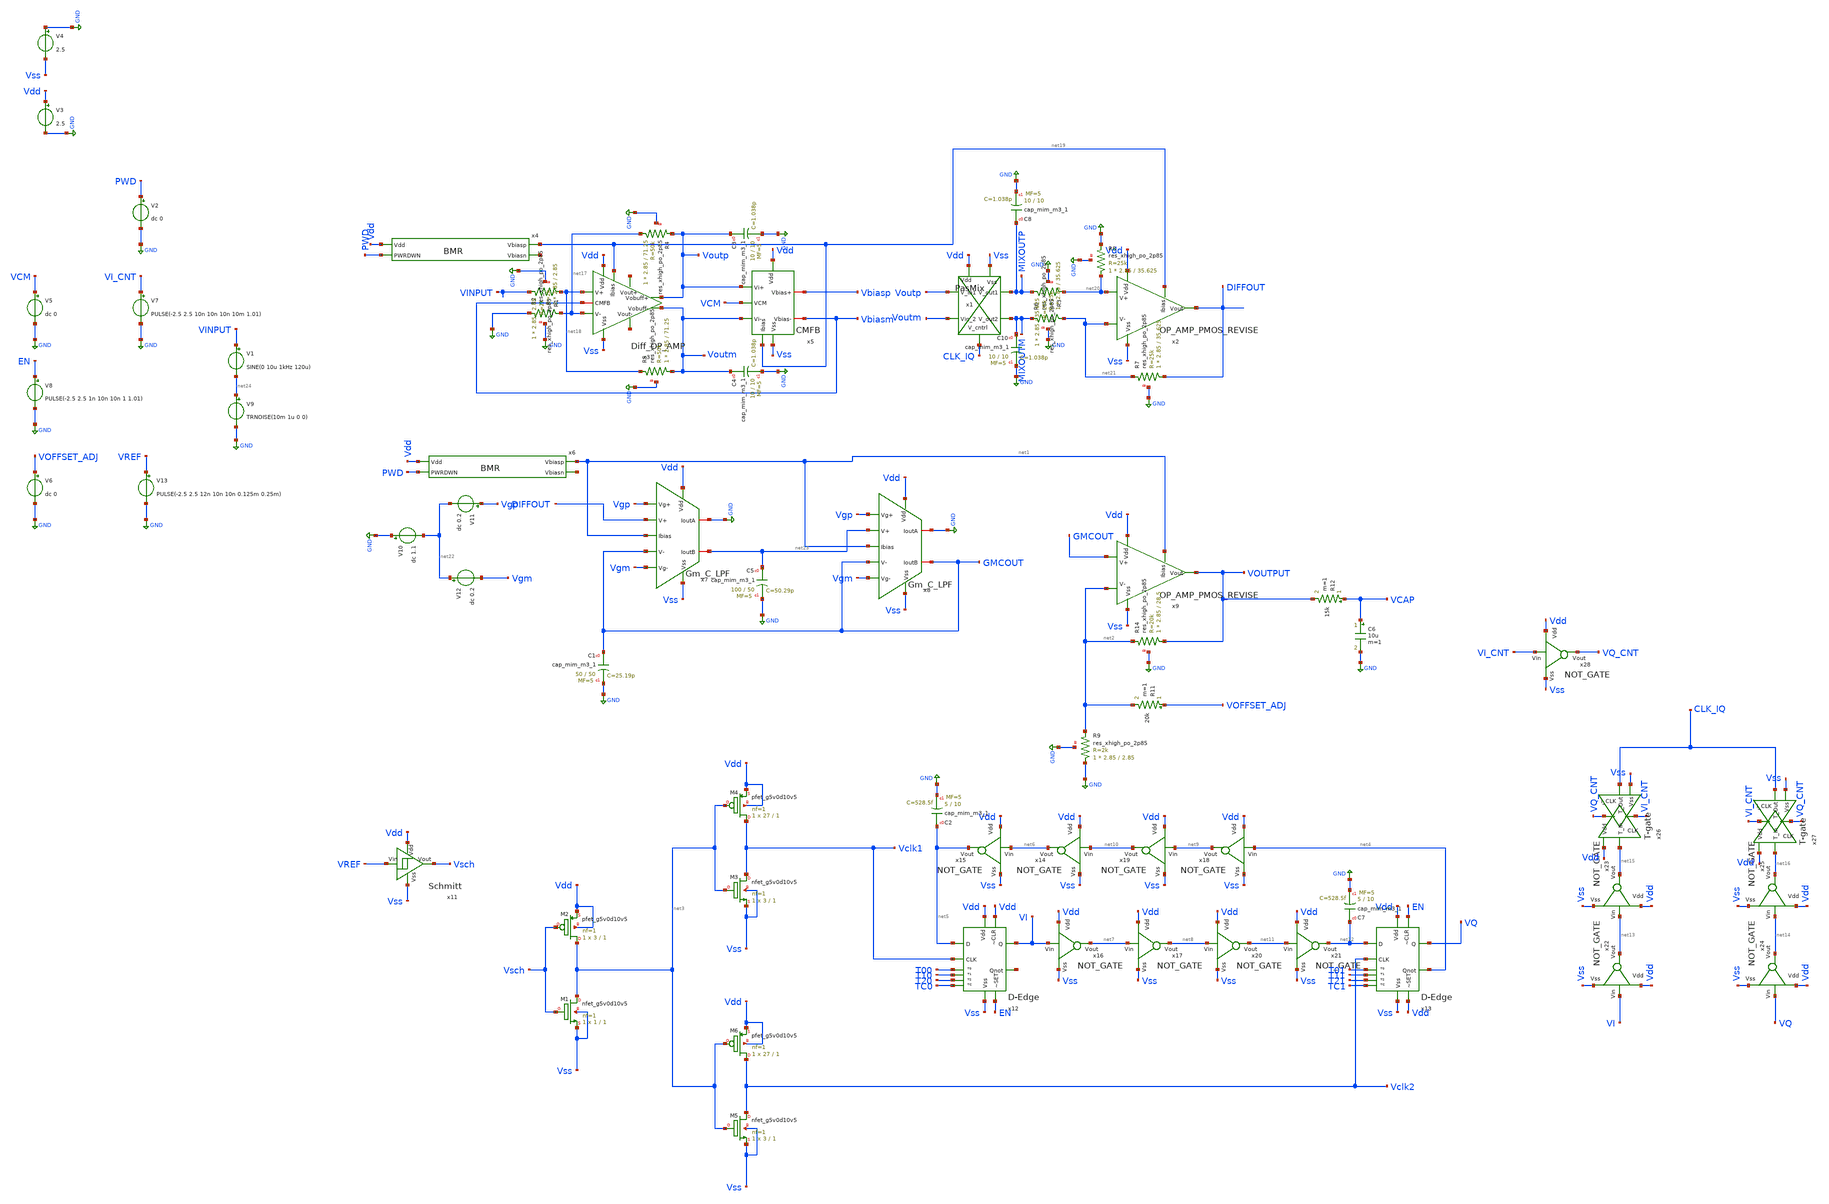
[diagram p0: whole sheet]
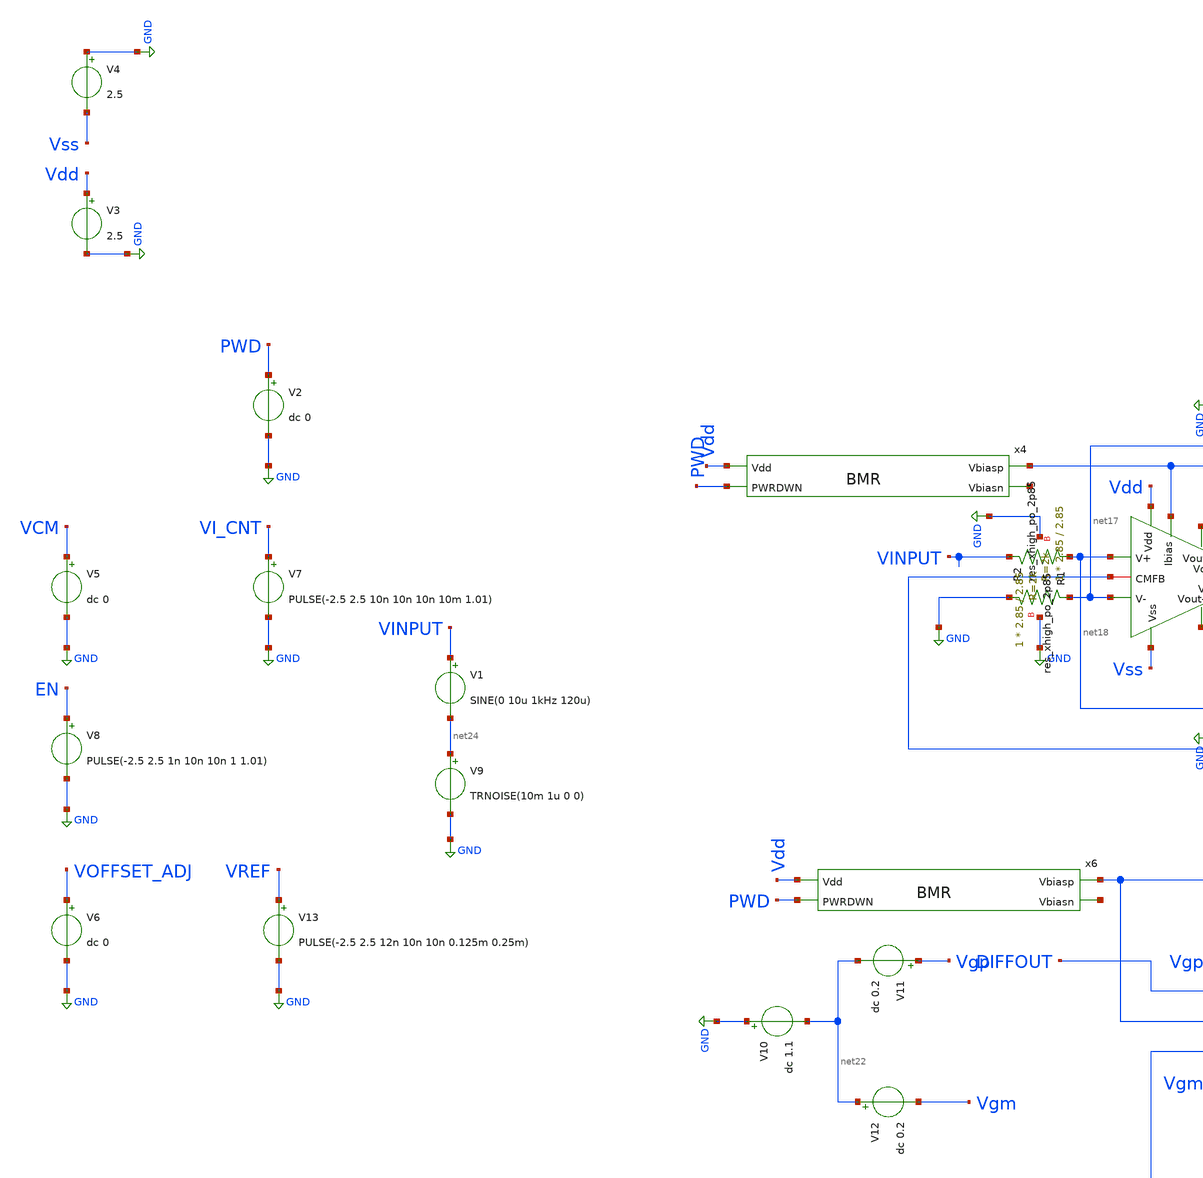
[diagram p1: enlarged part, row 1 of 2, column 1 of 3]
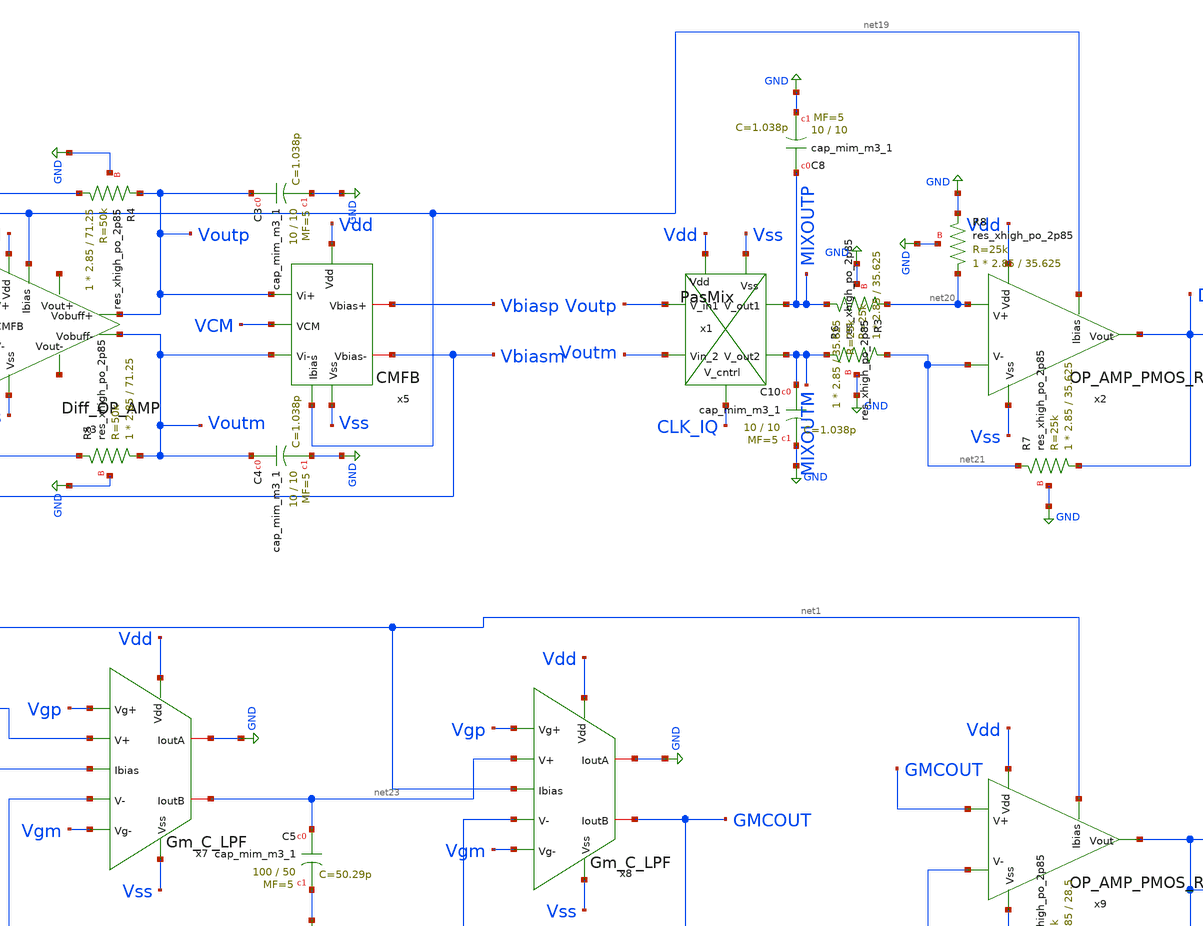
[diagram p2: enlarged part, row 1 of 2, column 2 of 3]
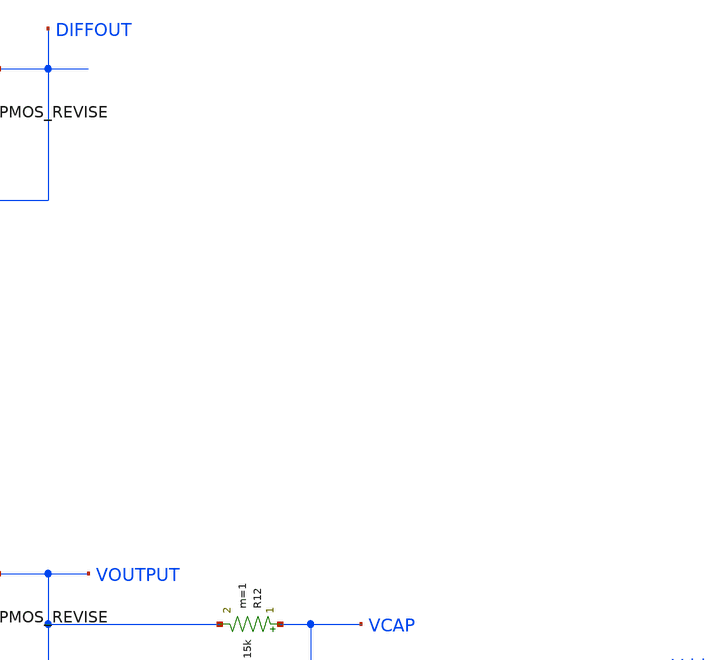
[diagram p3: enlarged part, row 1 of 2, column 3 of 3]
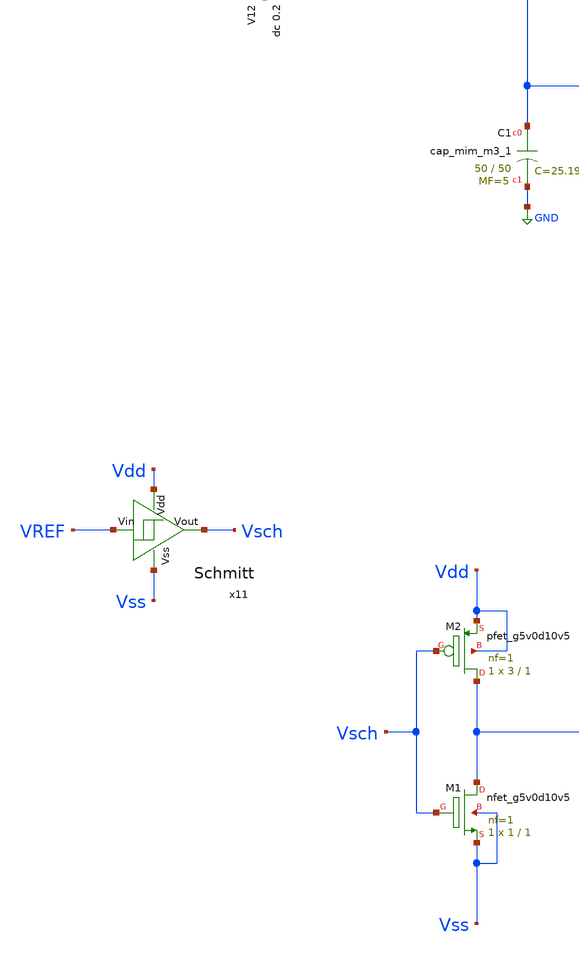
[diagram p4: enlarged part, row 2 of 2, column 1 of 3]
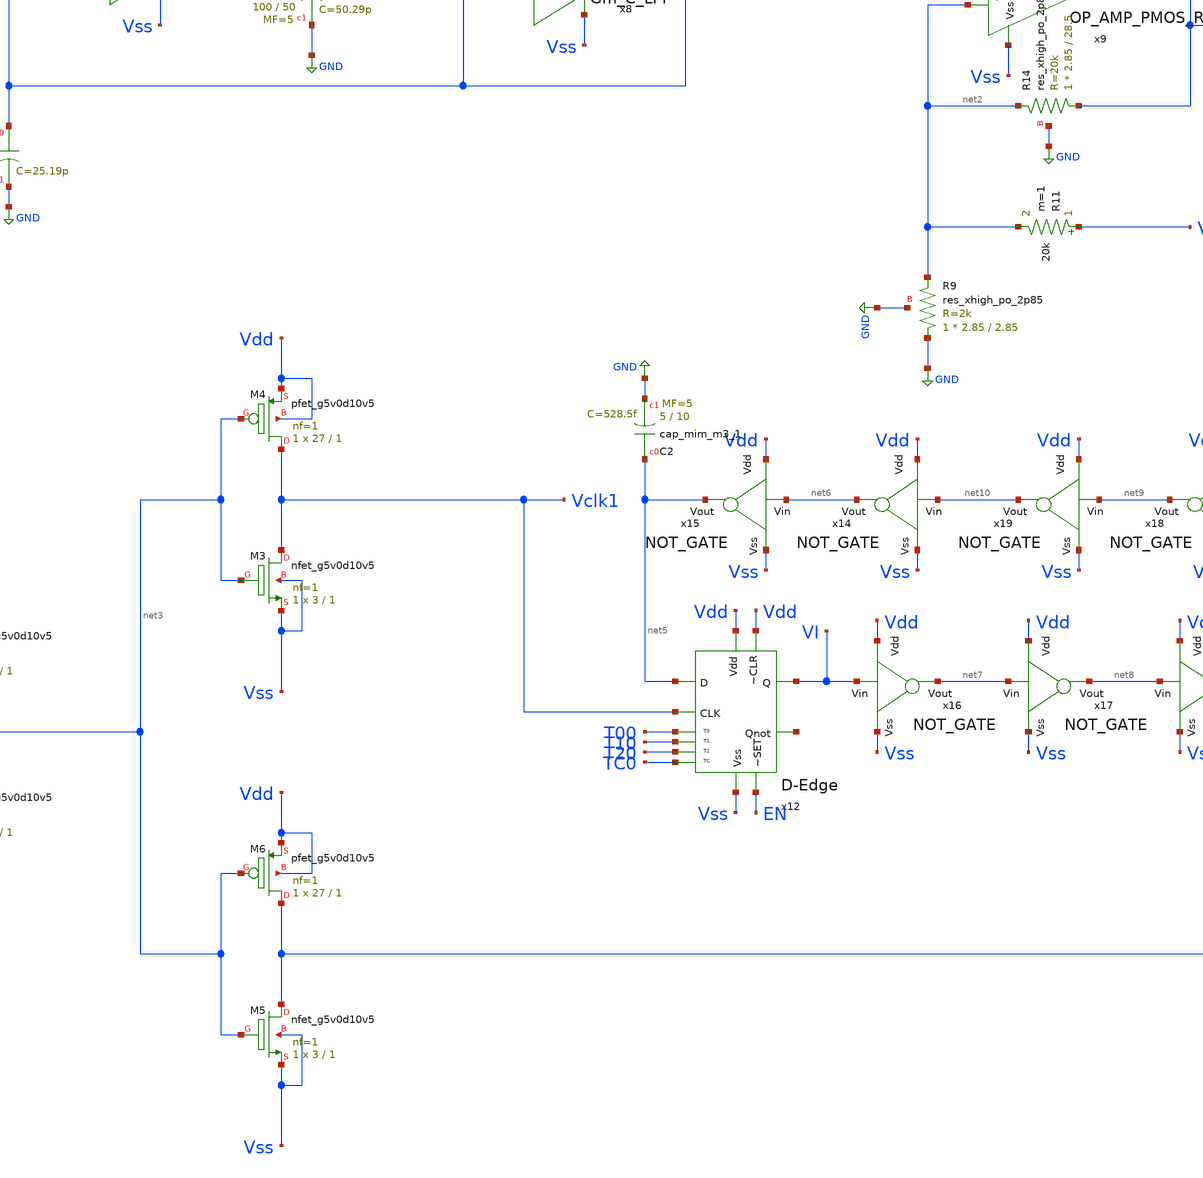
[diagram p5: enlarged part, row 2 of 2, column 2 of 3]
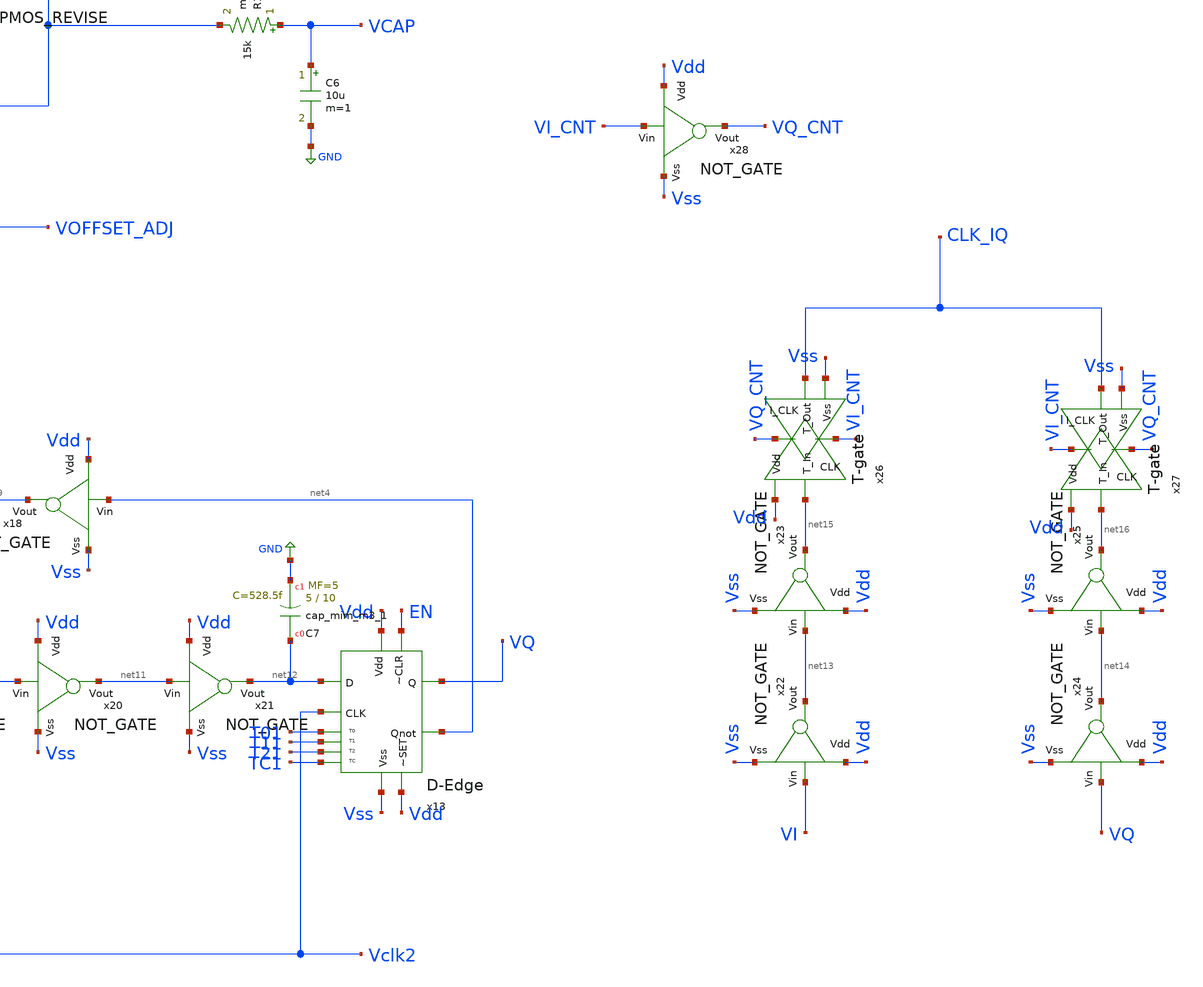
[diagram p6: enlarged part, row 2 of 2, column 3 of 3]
** sch_path: xschem/Lock_In_Amplifier.sch
**.subckt Lock_In_Amplifier
V1 VINPUT net24 SINE(0 10u 1kHz 120u)
V4 GND Vss 2.5
V3 Vdd GND 2.5
V5 VCM GND dc 0
x9 Vdd Vss net1 VOUTPUT GMCOUT net2 OP_AMP_PMOS_REVISE
V2 PWD GND dc 0
x11 Vdd Vss VREF Vsch Schmitt
V13 VREF GND PULSE(-2.5 2.5 12n 10n 10n 0.125m 0.25m)
XM1 net3 Vsch Vss Vss sky130_fd_pr__nfet_g5v0d10v5 L=1 W=1 nf=1 ad='int((1 + 1)/2) * 1 / 1 * 0.29' as='int((1 + 2)/2) * 1 / 1 * 0.29'
+ pd='2*int((1 + 1)/2) * (1 / 1 + 0.29)' ps='2*int((1 + 2)/2) * (1 / 1 + 0.29)' nrd='0.29 / 1 ' nrs='0.29 / 1 '
+ sa=0 sb=0 sd=0 mult=1 m=1
XM2 net3 Vsch Vdd Vdd sky130_fd_pr__pfet_g5v0d10v5 L=1 W=3 nf=1 ad='int((1 + 1)/2) * 3 / 1 * 0.29' as='int((1 + 2)/2) * 3 / 1 * 0.29'
+ pd='2*int((1 + 1)/2) * (3 / 1 + 0.29)' ps='2*int((1 + 2)/2) * (3 / 1 + 0.29)' nrd='0.29 / 3 ' nrs='0.29 / 3 '
+ sa=0 sb=0 sd=0 mult=1 m=1
XM3 Vclk1 net3 Vss Vss sky130_fd_pr__nfet_g5v0d10v5 L=1 W=3 nf=1 ad='int((1 + 1)/2) * 3 / 1 * 0.29' as='int((1 + 2)/2) * 3 / 1 * 0.29'
+ pd='2*int((1 + 1)/2) * (3 / 1 + 0.29)' ps='2*int((1 + 2)/2) * (3 / 1 + 0.29)' nrd='0.29 / 3 ' nrs='0.29 / 3 '
+ sa=0 sb=0 sd=0 mult=1 m=1
XM4 Vclk1 net3 Vdd Vdd sky130_fd_pr__pfet_g5v0d10v5 L=1 W=27 nf=1 ad='int((1 + 1)/2) * 27 / 1 * 0.29'
+ as='int((1 + 2)/2) * 27 / 1 * 0.29' pd='2*int((1 + 1)/2) * (27 / 1 + 0.29)' ps='2*int((1 + 2)/2) * (27 / 1 + 0.29)'
+ nrd='0.29 / 27 ' nrs='0.29 / 27 ' sa=0 sb=0 sd=0 mult=1 m=1
XM5 Vclk2 net3 Vss Vss sky130_fd_pr__nfet_g5v0d10v5 L=1 W=3 nf=1 ad='int((1 + 1)/2) * 3 / 1 * 0.29' as='int((1 + 2)/2) * 3 / 1 * 0.29'
+ pd='2*int((1 + 1)/2) * (3 / 1 + 0.29)' ps='2*int((1 + 2)/2) * (3 / 1 + 0.29)' nrd='0.29 / 3 ' nrs='0.29 / 3 '
+ sa=0 sb=0 sd=0 mult=1 m=1
XM6 Vclk2 net3 Vdd Vdd sky130_fd_pr__pfet_g5v0d10v5 L=1 W=27 nf=1 ad='int((1 + 1)/2) * 27 / 1 * 0.29'
+ as='int((1 + 2)/2) * 27 / 1 * 0.29' pd='2*int((1 + 1)/2) * (27 / 1 + 0.29)' ps='2*int((1 + 2)/2) * (27 / 1 + 0.29)'
+ nrd='0.29 / 27 ' nrs='0.29 / 27 ' sa=0 sb=0 sd=0 mult=1 m=1
x12 Vdd Vss Vdd EN VI net5 net25 Vclk1 TC0 T20 T10 T00 D-Edge
x13 Vdd Vss EN Vdd VQ net12 net4 Vclk2 TC1 T21 T11 T01 D-Edge
x14 Vdd net6 net10 Vss NOT_GATE
x15 Vdd net5 net6 Vss NOT_GATE
x16 Vdd net7 VI Vss NOT_GATE
x17 Vdd net8 net7 Vss NOT_GATE
x18 Vdd net9 net4 Vss NOT_GATE
x19 Vdd net10 net9 Vss NOT_GATE
x20 Vdd net11 net8 Vss NOT_GATE
x21 Vdd net12 net11 Vss NOT_GATE
V8 EN GND PULSE(-2.5 2.5 1n 10n 10n 1 1.01)
x22 Vdd net13 VI Vss NOT_GATE
x23 Vdd net15 net13 Vss NOT_GATE
x24 Vdd net14 VQ Vss NOT_GATE
x25 Vdd net16 net14 Vss NOT_GATE
x26 VQ_CNT net15 CLK_IQ Vdd Vss VI_CNT T-gate
x27 VI_CNT net16 CLK_IQ Vdd Vss VQ_CNT T-gate
x28 Vdd VQ_CNT VI_CNT Vss NOT_GATE
V6 VOFFSET_ADJ GND dc 0
x3 Vss Vbiasm net26 net27 net17 net18 Voutp Voutm net19 Vdd Diff_OP_AMP
x4 Vdd net19 net28 PWD BMR
x5 Vss Vbiasp Vbiasm Voutm Voutp VCM net19 Vdd CMFB
x1 Vdd CLK_IQ Vss MIXOUTP Voutp MIXOUTM Voutm PasMix
x2 Vdd Vss net19 DIFFOUT net20 net21 OP_AMP_PMOS_REVISE
V7 VI_CNT GND PULSE(-2.5 2.5 10n 10n 10n 10m 1.01)
V10 GND net22 dc 1.1
V11 Vgp net22 dc 0.2
x6 Vdd net1 net29 PWD BMR
x7 Vdd Vss Vgp Vgm GND net23 DIFFOUT GMCOUT net1 Gm_C_LPF
V12 net22 Vgm dc 0.2
x8 Vdd Vss Vgp Vgm GND GMCOUT net23 GMCOUT net1 Gm_C_LPF
R11 VOFFSET_ADJ net2 20k m=1
V9 net24 GND TRNOISE(10m 1u 0 0)
R12 VCAP VOUTPUT 15k m=1
C6 VCAP GND 10u m=1
XC3 Voutp GND sky130_fd_pr__cap_mim_m3_1 W=10 L=10 MF=5 m=5
XC4 Voutm GND sky130_fd_pr__cap_mim_m3_1 W=10 L=10 MF=5 m=5
XR4 net17 Voutp GND sky130_fd_pr__res_xhigh_po_2p85 L=71.25 mult=1 m=1
XR5 Voutm net18 GND sky130_fd_pr__res_xhigh_po_2p85 L=71.25 mult=1 m=1
XR2 net17 GND GND sky130_fd_pr__res_xhigh_po_2p85 L=2.85 mult=1 m=1
XR1 VINPUT net18 GND sky130_fd_pr__res_xhigh_po_2p85 L=2.85 mult=1 m=1
XC10 MIXOUTM GND sky130_fd_pr__cap_mim_m3_1 W=10 L=10 MF=5 m=5
XC8 MIXOUTP GND sky130_fd_pr__cap_mim_m3_1 W=10 L=10 MF=5 m=5
XC2 net5 GND sky130_fd_pr__cap_mim_m3_1 W=5 L=10 MF=5 m=5
XC7 net12 GND sky130_fd_pr__cap_mim_m3_1 W=5 L=10 MF=5 m=5
XR7 DIFFOUT net21 GND sky130_fd_pr__res_xhigh_po_2p85 L=35.625 mult=1 m=1
XR6 net21 MIXOUTM GND sky130_fd_pr__res_xhigh_po_2p85 L=35.625 mult=1 m=1
XR3 MIXOUTP net20 GND sky130_fd_pr__res_xhigh_po_2p85 L=35.625 mult=1 m=1
XR8 net20 GND GND sky130_fd_pr__res_xhigh_po_2p85 L=35.625 mult=1 m=1
XC5 net23 GND sky130_fd_pr__cap_mim_m3_1 W=100 L=50 MF=5 m=5
XC1 GMCOUT GND sky130_fd_pr__cap_mim_m3_1 W=50 L=50 MF=5 m=5
XR9 GND net2 GND sky130_fd_pr__res_xhigh_po_2p85 L=2.85 mult=1 m=1
XR14 VOUTPUT net2 GND sky130_fd_pr__res_xhigh_po_2p85 L=28.5 mult=1 m=1
**** begin user architecture code






.lib /foss/pdks/sky130A/libs.tech/combined/sky130.lib.spice tt
.options method = trap
.options rshunt = 1e12
.options retol = 0.01
.options vntol = 10u
.options abstol = 1n
.options trtol = 10
.options chgtol = 1e-10

.options sparse
.control
 save v(VOUTPUT) v(GMCOUT) v(VCAP)
 tran 1u 1 0 100u

 write Lock_In_Amplifier_TB_TT_NOISY_10UV_0.4_1S_FFT_NGSPICE.raw
 ***write Lock_In_Amplifier_TB_TT_1MV_IDEAL_NGSPICE.raw


 set appendwrite
.endc
.end


**** end user architecture code
**.ends

* expanding   symbol:  OP_AMP_PMOS_REVISE.sym # of pins=6
** sym_path: xschem/OP_AMP_PMOS_REVISE.sym
** sch_path: xschem/OP_AMP_PMOS_REVISE.sch
.subckt OP_AMP_PMOS_REVISE Vdd Vss Ibias Vout V+ V-
*.ipin V-
*.ipin V+
*.ipin Vdd
*.ipin Vss
*.ipin Ibias
*.opin Vout
XM3 net2 net1 Vss Vss sky130_fd_pr__nfet_g5v0d10v5 L=6 W=0.81 nf=1 ad='int((1 + 1)/2) * 0.81 / 1 * 0.29'
+ as='int((1 + 2)/2) * 0.81 / 1 * 0.29' pd='2*int((1 + 1)/2) * (0.81 / 1 + 0.29)' ps='2*int((1 + 2)/2) * (0.81 / 1 + 0.29)'
+ nrd='0.29 / 0.81 ' nrs='0.29 / 0.81 ' sa=0 sb=0 sd=0 mult=2 m=2
XM1 net2 V+ net3 net3 sky130_fd_pr__pfet_g5v0d10v5 L=3 W=80 nf=8 ad='int((8 + 1)/2) * 80 / 8 * 0.29'
+ as='int((8 + 2)/2) * 80 / 8 * 0.29' pd='2*int((8 + 1)/2) * (80 / 8 + 0.29)' ps='2*int((8 + 2)/2) * (80 / 8 + 0.29)'
+ nrd='0.29 / 80 ' nrs='0.29 / 80 ' sa=0 sb=0 sd=0 mult=4 m=4
XM2 net1 V- net3 net3 sky130_fd_pr__pfet_g5v0d10v5 L=3 W=80 nf=8 ad='int((8 + 1)/2) * 80 / 8 * 0.29'
+ as='int((8 + 2)/2) * 80 / 8 * 0.29' pd='2*int((8 + 1)/2) * (80 / 8 + 0.29)' ps='2*int((8 + 2)/2) * (80 / 8 + 0.29)'
+ nrd='0.29 / 80 ' nrs='0.29 / 80 ' sa=0 sb=0 sd=0 mult=4 m=4
XM4 net1 net1 Vss Vss sky130_fd_pr__nfet_g5v0d10v5 L=6 W=0.81 nf=1 ad='int((1 + 1)/2) * 0.81 / 1 * 0.29'
+ as='int((1 + 2)/2) * 0.81 / 1 * 0.29' pd='2*int((1 + 1)/2) * (0.81 / 1 + 0.29)' ps='2*int((1 + 2)/2) * (0.81 / 1 + 0.29)'
+ nrd='0.29 / 0.81 ' nrs='0.29 / 0.81 ' sa=0 sb=0 sd=0 mult=2 m=2
XM8 net4 net2 Vss Vss sky130_fd_pr__nfet_g5v0d10v5 L=3 W=14 nf=4 ad='int((4 + 1)/2) * 14 / 4 * 0.29'
+ as='int((4 + 2)/2) * 14 / 4 * 0.29' pd='2*int((4 + 1)/2) * (14 / 4 + 0.29)' ps='2*int((4 + 2)/2) * (14 / 4 + 0.29)'
+ nrd='0.29 / 14 ' nrs='0.29 / 14 ' sa=0 sb=0 sd=0 mult=2 m=2
XM5 net3 Ibias Vdd Vdd sky130_fd_pr__pfet_g5v0d10v5 L=3 W=31 nf=8 ad='int((8 + 1)/2) * 31 / 8 * 0.29'
+ as='int((8 + 2)/2) * 31 / 8 * 0.29' pd='2*int((8 + 1)/2) * (31 / 8 + 0.29)' ps='2*int((8 + 2)/2) * (31 / 8 + 0.29)'
+ nrd='0.29 / 31 ' nrs='0.29 / 31 ' sa=0 sb=0 sd=0 mult=2 m=2
XM6 net6 Ibias Vdd Vdd sky130_fd_pr__pfet_g5v0d10v5 L=3 W=31 nf=8 ad='int((8 + 1)/2) * 31 / 8 * 0.29'
+ as='int((8 + 2)/2) * 31 / 8 * 0.29' pd='2*int((8 + 1)/2) * (31 / 8 + 0.29)' ps='2*int((8 + 2)/2) * (31 / 8 + 0.29)'
+ nrd='0.29 / 31 ' nrs='0.29 / 31 ' sa=0 sb=0 sd=0 mult=30 m=30
XM7 net4 net4 net5 net5 sky130_fd_pr__pfet_g5v0d10v5 L=3 W=41.1 nf=4 ad='int((4 + 1)/2) * 41.1 / 4 * 0.29'
+ as='int((4 + 2)/2) * 41.1 / 4 * 0.29' pd='2*int((4 + 1)/2) * (41.1 / 4 + 0.29)' ps='2*int((4 + 2)/2) * (41.1 / 4 + 0.29)'
+ nrd='0.29 / 41.1 ' nrs='0.29 / 41.1 ' sa=0 sb=0 sd=0 mult=4 m=4
XM9 Vss net4 Vout Vout sky130_fd_pr__pfet_g5v0d10v5 L=3 W=41.1 nf=4 ad='int((4 + 1)/2) * 41.1 / 4 * 0.29'
+ as='int((4 + 2)/2) * 41.1 / 4 * 0.29' pd='2*int((4 + 1)/2) * (41.1 / 4 + 0.29)' ps='2*int((4 + 2)/2) * (41.1 / 4 + 0.29)'
+ nrd='0.29 / 41.1 ' nrs='0.29 / 41.1 ' sa=0 sb=0 sd=0 mult=4 m=4
XM10 net6 net6 net5 net5 sky130_fd_pr__nfet_g5v0d10v5 L=3 W=18 nf=4 ad='int((4 + 1)/2) * 18 / 4 * 0.29'
+ as='int((4 + 2)/2) * 18 / 4 * 0.29' pd='2*int((4 + 1)/2) * (18 / 4 + 0.29)' ps='2*int((4 + 2)/2) * (18 / 4 + 0.29)'
+ nrd='0.29 / 18 ' nrs='0.29 / 18 ' sa=0 sb=0 sd=0 mult=2 m=2
XM11 Vdd net6 Vout Vout sky130_fd_pr__nfet_g5v0d10v5 L=3 W=18 nf=4 ad='int((4 + 1)/2) * 18 / 4 * 0.29'
+ as='int((4 + 2)/2) * 18 / 4 * 0.29' pd='2*int((4 + 1)/2) * (18 / 4 + 0.29)' ps='2*int((4 + 2)/2) * (18 / 4 + 0.29)'
+ nrd='0.29 / 18 ' nrs='0.29 / 18 ' sa=0 sb=0 sd=0 mult=2 m=2
XC10 net2 net4 sky130_fd_pr__cap_mim_m3_1 W=10 L=10 MF=5 m=5
.ends


* expanding   symbol:  Schmitt.sym # of pins=4
** sym_path: xschem/Schmitt.sym
** sch_path: xschem/Schmitt.sch
.subckt Schmitt Vdd Vss Vin Vout
*.opin Vout
*.ipin Vin
*.ipin Vdd
*.ipin Vss
XM1 net1 Vin Vss Vss sky130_fd_pr__nfet_g5v0d10v5 L=0.5 W=2.92 nf=1 ad='int((1 + 1)/2) * 2.92 / 1 * 0.29'
+ as='int((1 + 2)/2) * 2.92 / 1 * 0.29' pd='2*int((1 + 1)/2) * (2.92 / 1 + 0.29)' ps='2*int((1 + 2)/2) * (2.92 / 1 + 0.29)'
+ nrd='0.29 / 2.92 ' nrs='0.29 / 2.92 ' sa=0 sb=0 sd=0 mult=1 m=1
XM5 net2 Vin Vdd Vdd sky130_fd_pr__pfet_g5v0d10v5 L=0.5 W=9.78 nf=1 ad='int((1 + 1)/2) * 9.78 / 1 * 0.29'
+ as='int((1 + 2)/2) * 9.78 / 1 * 0.29' pd='2*int((1 + 1)/2) * (9.78 / 1 + 0.29)' ps='2*int((1 + 2)/2) * (9.78 / 1 + 0.29)'
+ nrd='0.29 / 9.78 ' nrs='0.29 / 9.78 ' sa=0 sb=0 sd=0 mult=1 m=1
XM3 Vdd Vout net1 Vss sky130_fd_pr__nfet_g5v0d10v5 L=0.5 W=1 nf=1 ad='int((1 + 1)/2) * 1 / 1 * 0.29'
+ as='int((1 + 2)/2) * 1 / 1 * 0.29' pd='2*int((1 + 1)/2) * (1 / 1 + 0.29)' ps='2*int((1 + 2)/2) * (1 / 1 + 0.29)'
+ nrd='0.29 / 1 ' nrs='0.29 / 1 ' sa=0 sb=0 sd=0 mult=1 m=1
XM2 Vout Vin net1 Vss sky130_fd_pr__nfet_g5v0d10v5 L=0.5 W=4 nf=1 ad='int((1 + 1)/2) * 4 / 1 * 0.29'
+ as='int((1 + 2)/2) * 4 / 1 * 0.29' pd='2*int((1 + 1)/2) * (4 / 1 + 0.29)' ps='2*int((1 + 2)/2) * (4 / 1 + 0.29)'
+ nrd='0.29 / 4 ' nrs='0.29 / 4 ' sa=0 sb=0 sd=0 mult=1 m=1
XM6 Vss Vout net2 Vdd sky130_fd_pr__pfet_g5v0d10v5 L=0.5 W=3 nf=1 ad='int((1 + 1)/2) * 3 / 1 * 0.29'
+ as='int((1 + 2)/2) * 3 / 1 * 0.29' pd='2*int((1 + 1)/2) * (3 / 1 + 0.29)' ps='2*int((1 + 2)/2) * (3 / 1 + 0.29)'
+ nrd='0.29 / 3 ' nrs='0.29 / 3 ' sa=0 sb=0 sd=0 mult=1 m=1
XM4 Vout Vin net2 Vdd sky130_fd_pr__pfet_g5v0d10v5 L=0.5 W=12 nf=1 ad='int((1 + 1)/2) * 12 / 1 * 0.29'
+ as='int((1 + 2)/2) * 12 / 1 * 0.29' pd='2*int((1 + 1)/2) * (12 / 1 + 0.29)' ps='2*int((1 + 2)/2) * (12 / 1 + 0.29)'
+ nrd='0.29 / 12 ' nrs='0.29 / 12 ' sa=0 sb=0 sd=0 mult=1 m=1
.ends


* expanding   symbol:  D-Edge.sym # of pins=12
** sym_path: xschem/D-Edge.sym
** sch_path: xschem/D-Edge.sch
.subckt D-Edge Vdd Vss ~CLR ~SET Q D Qnot CLK TC T2 T1 T0
*.ipin D
*.ipin Vdd
*.ipin Vss
*.opin Q
*.opin Qnot
*.ipin ~CLR
*.ipin ~SET
*.ipin CLK
*.opin T0
*.opin T1
*.opin T2
*.opin TC
x1 CLK D T1 Vdd Vss CLK_I T-gate
x3 CLK_I T0 T1 Vdd Vss CLK T-gate
x4 CLK_I net1 T2 Vdd Vss CLK T-gate
x8 CLK Qnot T2 Vdd Vss CLK_I T-gate
x11 Vdd ~CLR T1 net1 Vss NAND_GATE
x2 Vdd ~SET net1 T0 Vss NAND_GATE
x5 Vdd ~CLR T2 Q Vss NAND_GATE
x7 Vdd ~SET Q Qnot Vss NAND_GATE
XM1 CLK_I CLK Vss Vss sky130_fd_pr__nfet_g5v0d10v5 L=1 W=3 nf=1 ad='int((1 + 1)/2) * 3 / 1 * 0.29' as='int((1 + 2)/2) * 3 / 1 * 0.29'
+ pd='2*int((1 + 1)/2) * (3 / 1 + 0.29)' ps='2*int((1 + 2)/2) * (3 / 1 + 0.29)' nrd='0.29 / 3 ' nrs='0.29 / 3 '
+ sa=0 sb=0 sd=0 mult=1 m=1
XM2 CLK_I CLK Vdd Vdd sky130_fd_pr__pfet_g5v0d10v5 L=1 W=27 nf=1 ad='int((1 + 1)/2) * 27 / 1 * 0.29'
+ as='int((1 + 2)/2) * 27 / 1 * 0.29' pd='2*int((1 + 1)/2) * (27 / 1 + 0.29)' ps='2*int((1 + 2)/2) * (27 / 1 + 0.29)'
+ nrd='0.29 / 27 ' nrs='0.29 / 27 ' sa=0 sb=0 sd=0 mult=1 m=1
XM3 TC CLK_I Vss Vss sky130_fd_pr__nfet_g5v0d10v5 L=1 W=3 nf=1 ad='int((1 + 1)/2) * 3 / 1 * 0.29' as='int((1 + 2)/2) * 3 / 1 * 0.29'
+ pd='2*int((1 + 1)/2) * (3 / 1 + 0.29)' ps='2*int((1 + 2)/2) * (3 / 1 + 0.29)' nrd='0.29 / 3 ' nrs='0.29 / 3 '
+ sa=0 sb=0 sd=0 mult=1 m=1
XM4 TC CLK_I Vdd Vdd sky130_fd_pr__pfet_g5v0d10v5 L=1 W=27 nf=1 ad='int((1 + 1)/2) * 27 / 1 * 0.29' as='int((1 + 2)/2) * 27 / 1 * 0.29'
+ pd='2*int((1 + 1)/2) * (27 / 1 + 0.29)' ps='2*int((1 + 2)/2) * (27 / 1 + 0.29)' nrd='0.29 / 27 ' nrs='0.29 / 27 '
+ sa=0 sb=0 sd=0 mult=1 m=1
.ends


* expanding   symbol:  NOT_GATE.sym # of pins=4
** sym_path: xschem/NOT_GATE.sym
** sch_path: xschem/NOT_GATE.sch
.subckt NOT_GATE Vdd Vout Vin Vss
*.opin Vout
*.ipin Vdd
*.ipin Vss
*.ipin Vin
XM1 Vout Vin Vss Vss sky130_fd_pr__nfet_g5v0d10v5 L=1 W=1 nf=1 ad='int((1 + 1)/2) * 1 / 1 * 0.29' as='int((1 + 2)/2) * 1 / 1 * 0.29'
+ pd='2*int((1 + 1)/2) * (1 / 1 + 0.29)' ps='2*int((1 + 2)/2) * (1 / 1 + 0.29)' nrd='0.29 / 1 ' nrs='0.29 / 1 '
+ sa=0 sb=0 sd=0 mult=1 m=1
XM2 Vout Vin Vdd Vdd sky130_fd_pr__pfet_g5v0d10v5 L=1 W=3 nf=1 ad='int((1 + 1)/2) * 3 / 1 * 0.29' as='int((1 + 2)/2) * 3 / 1 * 0.29'
+ pd='2*int((1 + 1)/2) * (3 / 1 + 0.29)' ps='2*int((1 + 2)/2) * (3 / 1 + 0.29)' nrd='0.29 / 3 ' nrs='0.29 / 3 '
+ sa=0 sb=0 sd=0 mult=1 m=1
.ends


* expanding   symbol:  T-gate.sym # of pins=6
** sym_path: xschem/T-gate.sym
** sch_path: xschem/T-gate.sch
.subckt T-gate I_CLK T_In T_Out Vdd Vss CLK
*.ipin T_In
*.opin T_Out
*.ipin Vdd
*.ipin Vss
*.ipin I_CLK
*.ipin CLK
XM1 T_In I_CLK T_Out Vdd sky130_fd_pr__pfet_g5v0d10v5 L=0.5 W=3 nf=1 ad='int((1 + 1)/2) * 3 / 1 * 0.29'
+ as='int((1 + 2)/2) * 3 / 1 * 0.29' pd='2*int((1 + 1)/2) * (3 / 1 + 0.29)' ps='2*int((1 + 2)/2) * (3 / 1 + 0.29)'
+ nrd='0.29 / 3 ' nrs='0.29 / 3 ' sa=0 sb=0 sd=0 mult=1 m=1
XM3 T_Out CLK T_In Vss sky130_fd_pr__nfet_g5v0d10v5 L=0.5 W=1 nf=1 ad='int((1 + 1)/2) * 1 / 1 * 0.29'
+ as='int((1 + 2)/2) * 1 / 1 * 0.29' pd='2*int((1 + 1)/2) * (1 / 1 + 0.29)' ps='2*int((1 + 2)/2) * (1 / 1 + 0.29)'
+ nrd='0.29 / 1 ' nrs='0.29 / 1 ' sa=0 sb=0 sd=0 mult=1 m=1
XM2 T_Out CLK T_Out Vdd sky130_fd_pr__pfet_g5v0d10v5 L=0.5 W=1.5 nf=1 ad='int((1 + 1)/2) * 1.5 / 1 * 0.29'
+ as='int((1 + 2)/2) * 1.5 / 1 * 0.29' pd='2*int((1 + 1)/2) * (1.5 / 1 + 0.29)' ps='2*int((1 + 2)/2) * (1.5 / 1 + 0.29)'
+ nrd='0.29 / 1.5 ' nrs='0.29 / 1.5 ' sa=0 sb=0 sd=0 mult=1 m=1
XM4 T_In CLK T_In Vdd sky130_fd_pr__pfet_g5v0d10v5 L=0.5 W=1.5 nf=1 ad='int((1 + 1)/2) * 1.5 / 1 * 0.29'
+ as='int((1 + 2)/2) * 1.5 / 1 * 0.29' pd='2*int((1 + 1)/2) * (1.5 / 1 + 0.29)' ps='2*int((1 + 2)/2) * (1.5 / 1 + 0.29)'
+ nrd='0.29 / 1.5 ' nrs='0.29 / 1.5 ' sa=0 sb=0 sd=0 mult=1 m=1
XM5 T_In I_CLK T_In Vss sky130_fd_pr__nfet_g5v0d10v5 L=0.5 W=0.5 nf=1 ad='int((1 + 1)/2) * 0.5 / 1 * 0.29'
+ as='int((1 + 2)/2) * 0.5 / 1 * 0.29' pd='2*int((1 + 1)/2) * (0.5 / 1 + 0.29)' ps='2*int((1 + 2)/2) * (0.5 / 1 + 0.29)'
+ nrd='0.29 / 0.5 ' nrs='0.29 / 0.5 ' sa=0 sb=0 sd=0 mult=1 m=1
XM6 T_Out I_CLK T_Out Vss sky130_fd_pr__nfet_g5v0d10v5 L=0.5 W=0.5 nf=1 ad='int((1 + 1)/2) * 0.5 / 1 * 0.29'
+ as='int((1 + 2)/2) * 0.5 / 1 * 0.29' pd='2*int((1 + 1)/2) * (0.5 / 1 + 0.29)' ps='2*int((1 + 2)/2) * (0.5 / 1 + 0.29)'
+ nrd='0.29 / 0.5 ' nrs='0.29 / 0.5 ' sa=0 sb=0 sd=0 mult=1 m=1
.ends


* expanding   symbol:  Diff_OP_AMP.sym # of pins=10
** sym_path: xschem/Diff_OP_AMP.sym
** sch_path: xschem/Diff_OP_AMP.sch
.subckt Diff_OP_AMP Vss CMFB Vout- Vout+ V- V+ Vobuff+ Vobuff- Ibias Vdd
*.opin Vout+
*.ipin Vdd
*.ipin Vss
*.ipin V+
*.ipin V-
*.opin Vout-
*.ipin Ibias
*.opin Vobuff-
*.opin Vobuff+
*.iopin CMFB
XM4 net1 Ibias Vdd Vdd sky130_fd_pr__pfet_g5v0d10v5 L=3 W=31 nf=8 ad='int((8 + 1)/2) * 31 / 8 * 0.29'
+ as='int((8 + 2)/2) * 31 / 8 * 0.29' pd='2*int((8 + 1)/2) * (31 / 8 + 0.29)' ps='2*int((8 + 2)/2) * (31 / 8 + 0.29)'
+ nrd='0.29 / 31 ' nrs='0.29 / 31 ' sa=0 sb=0 sd=0 mult=2 m=2
XM18 net2 V- net1 net1 sky130_fd_pr__pfet_g5v0d10v5 L=3 W=80 nf=8 ad='int((8 + 1)/2) * 80 / 8 * 0.29'
+ as='int((8 + 2)/2) * 80 / 8 * 0.29' pd='2*int((8 + 1)/2) * (80 / 8 + 0.29)' ps='2*int((8 + 2)/2) * (80 / 8 + 0.29)'
+ nrd='0.29 / 80 ' nrs='0.29 / 80 ' sa=0 sb=0 sd=0 mult=4 m=4
XM1 net3 V+ net1 net1 sky130_fd_pr__pfet_g5v0d10v5 L=3 W=80 nf=8 ad='int((8 + 1)/2) * 80 / 8 * 0.29'
+ as='int((8 + 2)/2) * 80 / 8 * 0.29' pd='2*int((8 + 1)/2) * (80 / 8 + 0.29)' ps='2*int((8 + 2)/2) * (80 / 8 + 0.29)'
+ nrd='0.29 / 80 ' nrs='0.29 / 80 ' sa=0 sb=0 sd=0 mult=4 m=4
XM11 net2 CMFB Vss Vss sky130_fd_pr__nfet_g5v0d10v5 L=6 W=0.81 nf=1 ad='int((1 + 1)/2) * 0.81 / 1 * 0.29'
+ as='int((1 + 2)/2) * 0.81 / 1 * 0.29' pd='2*int((1 + 1)/2) * (0.81 / 1 + 0.29)' ps='2*int((1 + 2)/2) * (0.81 / 1 + 0.29)'
+ nrd='0.29 / 0.81 ' nrs='0.29 / 0.81 ' sa=0 sb=0 sd=0 mult=2 m=2
XM3 net3 CMFB Vss Vss sky130_fd_pr__nfet_g5v0d10v5 L=6 W=0.81 nf=1 ad='int((1 + 1)/2) * 0.81 / 1 * 0.29'
+ as='int((1 + 2)/2) * 0.81 / 1 * 0.29' pd='2*int((1 + 1)/2) * (0.81 / 1 + 0.29)' ps='2*int((1 + 2)/2) * (0.81 / 1 + 0.29)'
+ nrd='0.29 / 0.81 ' nrs='0.29 / 0.81 ' sa=0 sb=0 sd=0 mult=2 m=2
XM13 Vout+ net2 Vss Vss sky130_fd_pr__nfet_g5v0d10v5 L=3 W=14 nf=2 ad='int((2 + 1)/2) * 14 / 2 * 0.29'
+ as='int((2 + 2)/2) * 14 / 2 * 0.29' pd='2*int((2 + 1)/2) * (14 / 2 + 0.29)' ps='2*int((2 + 2)/2) * (14 / 2 + 0.29)'
+ nrd='0.29 / 14 ' nrs='0.29 / 14 ' sa=0 sb=0 sd=0 mult=2 m=2
XM2 Vout- net3 Vss Vss sky130_fd_pr__nfet_g5v0d10v5 L=3 W=14 nf=2 ad='int((2 + 1)/2) * 14 / 2 * 0.29'
+ as='int((2 + 2)/2) * 14 / 2 * 0.29' pd='2*int((2 + 1)/2) * (14 / 2 + 0.29)' ps='2*int((2 + 2)/2) * (14 / 2 + 0.29)'
+ nrd='0.29 / 14 ' nrs='0.29 / 14 ' sa=0 sb=0 sd=0 mult=2 m=2
XM5 net5 Ibias Vdd Vdd sky130_fd_pr__pfet_g5v0d10v5 L=3 W=31 nf=8 ad='int((8 + 1)/2) * 31 / 8 * 0.29'
+ as='int((8 + 2)/2) * 31 / 8 * 0.29' pd='2*int((8 + 1)/2) * (31 / 8 + 0.29)' ps='2*int((8 + 2)/2) * (31 / 8 + 0.29)'
+ nrd='0.29 / 31 ' nrs='0.29 / 31 ' sa=0 sb=0 sd=0 mult=30 m=30
XM6 net7 Ibias Vdd Vdd sky130_fd_pr__pfet_g5v0d10v5 L=3 W=31 nf=8 ad='int((8 + 1)/2) * 31 / 8 * 0.29'
+ as='int((8 + 2)/2) * 31 / 8 * 0.29' pd='2*int((8 + 1)/2) * (31 / 8 + 0.29)' ps='2*int((8 + 2)/2) * (31 / 8 + 0.29)'
+ nrd='0.29 / 31 ' nrs='0.29 / 31 ' sa=0 sb=0 sd=0 mult=30 m=30
XM8 Vout+ Vout+ net4 net4 sky130_fd_pr__pfet_g5v0d10v5 L=3 W=41.1 nf=4 ad='int((4 + 1)/2) * 41.1 / 4 * 0.29'
+ as='int((4 + 2)/2) * 41.1 / 4 * 0.29' pd='2*int((4 + 1)/2) * (41.1 / 4 + 0.29)' ps='2*int((4 + 2)/2) * (41.1 / 4 + 0.29)'
+ nrd='0.29 / 41.1 ' nrs='0.29 / 41.1 ' sa=0 sb=0 sd=0 mult=4 m=4
XM7 Vss Vout+ Vobuff- Vobuff- sky130_fd_pr__pfet_g5v0d10v5 L=3 W=41.1 nf=4 ad='int((4 + 1)/2) * 41.1 / 4 * 0.29'
+ as='int((4 + 2)/2) * 41.1 / 4 * 0.29' pd='2*int((4 + 1)/2) * (41.1 / 4 + 0.29)' ps='2*int((4 + 2)/2) * (41.1 / 4 + 0.29)'
+ nrd='0.29 / 41.1 ' nrs='0.29 / 41.1 ' sa=0 sb=0 sd=0 mult=4 m=4
XM9 Vss Vout- Vobuff+ Vobuff+ sky130_fd_pr__pfet_g5v0d10v5 L=3 W=41.1 nf=4 ad='int((4 + 1)/2) * 41.1 / 4 * 0.29'
+ as='int((4 + 2)/2) * 41.1 / 4 * 0.29' pd='2*int((4 + 1)/2) * (41.1 / 4 + 0.29)' ps='2*int((4 + 2)/2) * (41.1 / 4 + 0.29)'
+ nrd='0.29 / 41.1 ' nrs='0.29 / 41.1 ' sa=0 sb=0 sd=0 mult=4 m=4
XM12 Vout- Vout- net6 net6 sky130_fd_pr__pfet_g5v0d10v5 L=3 W=41.1 nf=4 ad='int((4 + 1)/2) * 41.1 / 4 * 0.29'
+ as='int((4 + 2)/2) * 41.1 / 4 * 0.29' pd='2*int((4 + 1)/2) * (41.1 / 4 + 0.29)' ps='2*int((4 + 2)/2) * (41.1 / 4 + 0.29)'
+ nrd='0.29 / 41.1 ' nrs='0.29 / 41.1 ' sa=0 sb=0 sd=0 mult=4 m=4
XM16 net5 net5 net4 net4 sky130_fd_pr__nfet_g5v0d10v5 L=3 W=18 nf=4 ad='int((4 + 1)/2) * 18 / 4 * 0.29'
+ as='int((4 + 2)/2) * 18 / 4 * 0.29' pd='2*int((4 + 1)/2) * (18 / 4 + 0.29)' ps='2*int((4 + 2)/2) * (18 / 4 + 0.29)'
+ nrd='0.29 / 18 ' nrs='0.29 / 18 ' sa=0 sb=0 sd=0 mult=2 m=2
XM14 Vdd net5 Vobuff- Vobuff- sky130_fd_pr__nfet_g5v0d10v5 L=3 W=18 nf=4 ad='int((4 + 1)/2) * 18 / 4 * 0.29'
+ as='int((4 + 2)/2) * 18 / 4 * 0.29' pd='2*int((4 + 1)/2) * (18 / 4 + 0.29)' ps='2*int((4 + 2)/2) * (18 / 4 + 0.29)'
+ nrd='0.29 / 18 ' nrs='0.29 / 18 ' sa=0 sb=0 sd=0 mult=2 m=2
XM10 Vdd net7 Vobuff+ Vobuff+ sky130_fd_pr__nfet_g5v0d10v5 L=3 W=18 nf=4 ad='int((4 + 1)/2) * 18 / 4 * 0.29'
+ as='int((4 + 2)/2) * 18 / 4 * 0.29' pd='2*int((4 + 1)/2) * (18 / 4 + 0.29)' ps='2*int((4 + 2)/2) * (18 / 4 + 0.29)'
+ nrd='0.29 / 18 ' nrs='0.29 / 18 ' sa=0 sb=0 sd=0 mult=2 m=2
XM15 net7 net7 net6 net6 sky130_fd_pr__nfet_g5v0d10v5 L=3 W=18 nf=4 ad='int((4 + 1)/2) * 18 / 4 * 0.29'
+ as='int((4 + 2)/2) * 18 / 4 * 0.29' pd='2*int((4 + 1)/2) * (18 / 4 + 0.29)' ps='2*int((4 + 2)/2) * (18 / 4 + 0.29)'
+ nrd='0.29 / 18 ' nrs='0.29 / 18 ' sa=0 sb=0 sd=0 mult=2 m=2
XC10 net2 Vout+ sky130_fd_pr__cap_mim_m3_1 W=10 L=10 MF=5 m=5
XC1 net3 Vout- sky130_fd_pr__cap_mim_m3_1 W=10 L=10 MF=5 m=5
.ends


* expanding   symbol:  BMR.sym # of pins=4
** sym_path: xschem/BMR.sym
** sch_path: xschem/BMR.sch
.subckt BMR Vdd Vbiasp Vbiasn PWRDWN
*.ipin Vdd
*.opin Vbiasn
*.opin Vbiasp
*.ipin PWRDWN
XM3 Vbiasn Vbiasn GND GND sky130_fd_pr__nfet_g5v0d10v5 L=3 W=1.4 nf=1 ad='int((1 + 1)/2) * 1.4 / 1 * 0.29'
+ as='int((1 + 2)/2) * 1.4 / 1 * 0.29' pd='2*int((1 + 1)/2) * (1.4 / 1 + 0.29)' ps='2*int((1 + 2)/2) * (1.4 / 1 + 0.29)'
+ nrd='0.29 / 1.4 ' nrs='0.29 / 1.4 ' sa=0 sb=0 sd=0 mult=1 m=1
XM1 Vbiasp Vbiasp Vdd Vdd sky130_fd_pr__pfet_g5v0d10v5 L=3 W=31 nf=8 ad='int((8 + 1)/2) * 31 / 8 * 0.29'
+ as='int((8 + 2)/2) * 31 / 8 * 0.29' pd='2*int((8 + 1)/2) * (31 / 8 + 0.29)' ps='2*int((8 + 2)/2) * (31 / 8 + 0.29)'
+ nrd='0.29 / 31 ' nrs='0.29 / 31 ' sa=0 sb=0 sd=0 mult=2 m=2
XM2 Vbiasn Vbiasp Vdd Vdd sky130_fd_pr__pfet_g5v0d10v5 L=3 W=31 nf=8 ad='int((8 + 1)/2) * 31 / 8 * 0.29'
+ as='int((8 + 2)/2) * 31 / 8 * 0.29' pd='2*int((8 + 1)/2) * (31 / 8 + 0.29)' ps='2*int((8 + 2)/2) * (31 / 8 + 0.29)'
+ nrd='0.29 / 31 ' nrs='0.29 / 31 ' sa=0 sb=0 sd=0 mult=2 m=2
XM11 net1 PWRUP Vdd Vdd sky130_fd_pr__pfet_g5v0d10v5 L=10 W=1 nf=1 ad='int((1 + 1)/2) * 1 / 1 * 0.29'
+ as='int((1 + 2)/2) * 1 / 1 * 0.29' pd='2*int((1 + 1)/2) * (1 / 1 + 0.29)' ps='2*int((1 + 2)/2) * (1 / 1 + 0.29)'
+ nrd='0.29 / 1 ' nrs='0.29 / 1 ' sa=0 sb=0 sd=0 mult=1 m=1
XM4 Vbiasp Vbiasn net2 GND sky130_fd_pr__nfet_g5v0d10v5 L=3 W=1.4 nf=1 ad='int((1 + 1)/2) * 1.4 / 1 * 0.29'
+ as='int((1 + 2)/2) * 1.4 / 1 * 0.29' pd='2*int((1 + 1)/2) * (1.4 / 1 + 0.29)' ps='2*int((1 + 2)/2) * (1.4 / 1 + 0.29)'
+ nrd='0.29 / 1.4 ' nrs='0.29 / 1.4 ' sa=0 sb=0 sd=0 mult=2 m=2
XM5 net1 Vbiasn GND GND sky130_fd_pr__nfet_g5v0d10v5 L=3 W=1.4 nf=1 ad='int((1 + 1)/2) * 1.4 / 1 * 0.29'
+ as='int((1 + 2)/2) * 1.4 / 1 * 0.29' pd='2*int((1 + 1)/2) * (1.4 / 1 + 0.29)' ps='2*int((1 + 2)/2) * (1.4 / 1 + 0.29)'
+ nrd='0.29 / 1.4 ' nrs='0.29 / 1.4 ' sa=0 sb=0 sd=0 mult=1 m=1
XM7 net3 net1 Vbiasn GND sky130_fd_pr__nfet_g5v0d10v5 L=1 W=20 nf=1 ad='int((1 + 1)/2) * 20 / 1 * 0.29'
+ as='int((1 + 2)/2) * 20 / 1 * 0.29' pd='2*int((1 + 1)/2) * (20 / 1 + 0.29)' ps='2*int((1 + 2)/2) * (20 / 1 + 0.29)'
+ nrd='0.29 / 20 ' nrs='0.29 / 20 ' sa=0 sb=0 sd=0 mult=1 m=1
x1 Vdd PWRUP PWRDWN GND NOT_GATE
XM12 Vbiasp PWRUP net3 GND sky130_fd_pr__nfet_g5v0d10v5 L=1 W=20 nf=1 ad='int((1 + 1)/2) * 20 / 1 * 0.29'
+ as='int((1 + 2)/2) * 20 / 1 * 0.29' pd='2*int((1 + 1)/2) * (20 / 1 + 0.29)' ps='2*int((1 + 2)/2) * (20 / 1 + 0.29)'
+ nrd='0.29 / 20 ' nrs='0.29 / 20 ' sa=0 sb=0 sd=0 mult=1 m=1
XM9 Vbiasp PWRUP Vdd Vdd sky130_fd_pr__pfet_g5v0d10v5 L=1 W=3 nf=1 ad='int((1 + 1)/2) * 3 / 1 * 0.29'
+ as='int((1 + 2)/2) * 3 / 1 * 0.29' pd='2*int((1 + 1)/2) * (3 / 1 + 0.29)' ps='2*int((1 + 2)/2) * (3 / 1 + 0.29)'
+ nrd='0.29 / 3 ' nrs='0.29 / 3 ' sa=0 sb=0 sd=0 mult=1 m=1
XM10 Vbiasn PWRDWN GND GND sky130_fd_pr__nfet_g5v0d10v5 L=1 W=1 nf=1 ad='int((1 + 1)/2) * 1 / 1 * 0.29'
+ as='int((1 + 2)/2) * 1 / 1 * 0.29' pd='2*int((1 + 1)/2) * (1 / 1 + 0.29)' ps='2*int((1 + 2)/2) * (1 / 1 + 0.29)'
+ nrd='0.29 / 1 ' nrs='0.29 / 1 ' sa=0 sb=0 sd=0 mult=1 m=1
XR5 GND net2 GND sky130_fd_pr__res_xhigh_po_2p85 L=71.25 mult=1 m=1
XC10 Vdd net1 sky130_fd_pr__cap_mim_m3_1 W=10 L=10 MF=5 m=5
XC2 Vdd Vbiasp sky130_fd_pr__cap_mim_m3_1 W=10 L=10 MF=5 m=5
XC1 Vbiasn GND sky130_fd_pr__cap_mim_m3_1 W=10 L=10 MF=5 m=5
.ends


* expanding   symbol:  CMFB.sym # of pins=8
** sym_path: xschem/CMFB.sym
** sch_path: xschem/CMFB.sch
.subckt CMFB Vss Vbias+ Vbias- Vi- Vi+ VCM Ibias Vdd
*.ipin VCM
*.ipin Vss
*.ipin Vdd
*.ipin Vi+
*.ipin Vi-
*.ipin Ibias
*.iopin Vbias+
*.iopin Vbias-
XM9 net1 Ibias Vdd Vdd sky130_fd_pr__pfet_g5v0d10v5 L=3 W=31 nf=8 ad='int((8 + 1)/2) * 31 / 8 * 0.29'
+ as='int((8 + 2)/2) * 31 / 8 * 0.29' pd='2*int((8 + 1)/2) * (31 / 8 + 0.29)' ps='2*int((8 + 2)/2) * (31 / 8 + 0.29)'
+ nrd='0.29 / 31 ' nrs='0.29 / 31 ' sa=0 sb=0 sd=0 mult=1 m=1
XM1 net2 Ibias Vdd Vdd sky130_fd_pr__pfet_g5v0d10v5 L=3 W=31 nf=8 ad='int((8 + 1)/2) * 31 / 8 * 0.29'
+ as='int((8 + 2)/2) * 31 / 8 * 0.29' pd='2*int((8 + 1)/2) * (31 / 8 + 0.29)' ps='2*int((8 + 2)/2) * (31 / 8 + 0.29)'
+ nrd='0.29 / 31 ' nrs='0.29 / 31 ' sa=0 sb=0 sd=0 mult=1 m=1
XM5 Vbias- Vi+ net1 net1 sky130_fd_pr__pfet_g5v0d10v5 L=1 W=28 nf=4 ad='int((4 + 1)/2) * 28 / 4 * 0.29'
+ as='int((4 + 2)/2) * 28 / 4 * 0.29' pd='2*int((4 + 1)/2) * (28 / 4 + 0.29)' ps='2*int((4 + 2)/2) * (28 / 4 + 0.29)'
+ nrd='0.29 / 28 ' nrs='0.29 / 28 ' sa=0 sb=0 sd=0 mult=2 m=2
XM2 Vbias+ VCM net2 net2 sky130_fd_pr__pfet_g5v0d10v5 L=1 W=28 nf=4 ad='int((4 + 1)/2) * 28 / 4 * 0.29'
+ as='int((4 + 2)/2) * 28 / 4 * 0.29' pd='2*int((4 + 1)/2) * (28 / 4 + 0.29)' ps='2*int((4 + 2)/2) * (28 / 4 + 0.29)'
+ nrd='0.29 / 28 ' nrs='0.29 / 28 ' sa=0 sb=0 sd=0 mult=2 m=2
XM4 Vbias+ VCM net1 net1 sky130_fd_pr__pfet_g5v0d10v5 L=1 W=28 nf=4 ad='int((4 + 1)/2) * 28 / 4 * 0.29'
+ as='int((4 + 2)/2) * 28 / 4 * 0.29' pd='2*int((4 + 1)/2) * (28 / 4 + 0.29)' ps='2*int((4 + 2)/2) * (28 / 4 + 0.29)'
+ nrd='0.29 / 28 ' nrs='0.29 / 28 ' sa=0 sb=0 sd=0 mult=2 m=2
XM3 Vbias- Vi- net2 net2 sky130_fd_pr__pfet_g5v0d10v5 L=1 W=28 nf=4 ad='int((4 + 1)/2) * 28 / 4 * 0.29'
+ as='int((4 + 2)/2) * 28 / 4 * 0.29' pd='2*int((4 + 1)/2) * (28 / 4 + 0.29)' ps='2*int((4 + 2)/2) * (28 / 4 + 0.29)'
+ nrd='0.29 / 28 ' nrs='0.29 / 28 ' sa=0 sb=0 sd=0 mult=2 m=2
XM6 Vbias+ Vbias+ Vss Vss sky130_fd_pr__nfet_g5v0d10v5 L=6 W=0.81 nf=1 ad='int((1 + 1)/2) * 0.81 / 1 * 0.29'
+ as='int((1 + 2)/2) * 0.81 / 1 * 0.29' pd='2*int((1 + 1)/2) * (0.81 / 1 + 0.29)' ps='2*int((1 + 2)/2) * (0.81 / 1 + 0.29)'
+ nrd='0.29 / 0.81 ' nrs='0.29 / 0.81 ' sa=0 sb=0 sd=0 mult=2 m=2
XM7 Vbias- Vbias- Vss Vss sky130_fd_pr__nfet_g5v0d10v5 L=6 W=0.81 nf=1 ad='int((1 + 1)/2) * 0.81 / 1 * 0.29'
+ as='int((1 + 2)/2) * 0.81 / 1 * 0.29' pd='2*int((1 + 1)/2) * (0.81 / 1 + 0.29)' ps='2*int((1 + 2)/2) * (0.81 / 1 + 0.29)'
+ nrd='0.29 / 0.81 ' nrs='0.29 / 0.81 ' sa=0 sb=0 sd=0 mult=2 m=2
.ends


* expanding   symbol:  PasMix.sym # of pins=7
** sym_path: xschem/PasMix.sym
** sch_path: xschem/PasMix.sch
.subckt PasMix Vdd V_cntrl Vss V_out1 V_in1 V_out2 Vin_2
*.ipin V_in1
*.ipin Vin_2
*.opin V_out1
*.opin V_out2
*.ipin Vdd
*.ipin Vss
*.ipin V_cntrl
x1 V_Invert V_in1 V_out1 Vdd Vss V_CLK T-gate
x2 V_Invert Vin_2 V_out2 Vdd Vss V_CLK T-gate
x3 V_CLK Vin_2 V_out1 Vdd Vss V_Invert T-gate
x4 V_CLK V_in1 V_out2 Vdd Vss V_Invert T-gate
XM3 net1 V_cntrl Vss Vss sky130_fd_pr__nfet_g5v0d10v5 L=1 W=1 nf=1 ad='int((1 + 1)/2) * 1 / 1 * 0.29'
+ as='int((1 + 2)/2) * 1 / 1 * 0.29' pd='2*int((1 + 1)/2) * (1 / 1 + 0.29)' ps='2*int((1 + 2)/2) * (1 / 1 + 0.29)'
+ nrd='0.29 / 1 ' nrs='0.29 / 1 ' sa=0 sb=0 sd=0 mult=1 m=1
XM4 net1 V_cntrl Vdd Vdd sky130_fd_pr__pfet_g5v0d10v5 L=1 W=3 nf=1 ad='int((1 + 1)/2) * 3 / 1 * 0.29'
+ as='int((1 + 2)/2) * 3 / 1 * 0.29' pd='2*int((1 + 1)/2) * (3 / 1 + 0.29)' ps='2*int((1 + 2)/2) * (3 / 1 + 0.29)'
+ nrd='0.29 / 3 ' nrs='0.29 / 3 ' sa=0 sb=0 sd=0 mult=1 m=1
XM5 V_CLK net1 Vss Vss sky130_fd_pr__nfet_g5v0d10v5 L=1 W=3 nf=1 ad='int((1 + 1)/2) * 3 / 1 * 0.29' as='int((1 + 2)/2) * 3 / 1 * 0.29'
+ pd='2*int((1 + 1)/2) * (3 / 1 + 0.29)' ps='2*int((1 + 2)/2) * (3 / 1 + 0.29)' nrd='0.29 / 3 ' nrs='0.29 / 3 '
+ sa=0 sb=0 sd=0 mult=1 m=1
XM6 V_CLK net1 Vdd Vdd sky130_fd_pr__pfet_g5v0d10v5 L=1 W=27 nf=1 ad='int((1 + 1)/2) * 27 / 1 * 0.29'
+ as='int((1 + 2)/2) * 27 / 1 * 0.29' pd='2*int((1 + 1)/2) * (27 / 1 + 0.29)' ps='2*int((1 + 2)/2) * (27 / 1 + 0.29)'
+ nrd='0.29 / 27 ' nrs='0.29 / 27 ' sa=0 sb=0 sd=0 mult=1 m=1
XM7 net2 net1 Vss Vss sky130_fd_pr__nfet_g5v0d10v5 L=1 W=3 nf=1 ad='int((1 + 1)/2) * 3 / 1 * 0.29' as='int((1 + 2)/2) * 3 / 1 * 0.29'
+ pd='2*int((1 + 1)/2) * (3 / 1 + 0.29)' ps='2*int((1 + 2)/2) * (3 / 1 + 0.29)' nrd='0.29 / 3 ' nrs='0.29 / 3 '
+ sa=0 sb=0 sd=0 mult=1 m=1
XM8 net2 net1 Vdd Vdd sky130_fd_pr__pfet_g5v0d10v5 L=1 W=27 nf=1 ad='int((1 + 1)/2) * 27 / 1 * 0.29'
+ as='int((1 + 2)/2) * 27 / 1 * 0.29' pd='2*int((1 + 1)/2) * (27 / 1 + 0.29)' ps='2*int((1 + 2)/2) * (27 / 1 + 0.29)'
+ nrd='0.29 / 27 ' nrs='0.29 / 27 ' sa=0 sb=0 sd=0 mult=1 m=1
XM9 V_Invert net2 Vss Vss sky130_fd_pr__nfet_g5v0d10v5 L=1 W=3 nf=1 ad='int((1 + 1)/2) * 3 / 1 * 0.29'
+ as='int((1 + 2)/2) * 3 / 1 * 0.29' pd='2*int((1 + 1)/2) * (3 / 1 + 0.29)' ps='2*int((1 + 2)/2) * (3 / 1 + 0.29)'
+ nrd='0.29 / 3 ' nrs='0.29 / 3 ' sa=0 sb=0 sd=0 mult=1 m=1
XM10 V_Invert net2 Vdd Vdd sky130_fd_pr__pfet_g5v0d10v5 L=1 W=27 nf=1 ad='int((1 + 1)/2) * 27 / 1 * 0.29'
+ as='int((1 + 2)/2) * 27 / 1 * 0.29' pd='2*int((1 + 1)/2) * (27 / 1 + 0.29)' ps='2*int((1 + 2)/2) * (27 / 1 + 0.29)'
+ nrd='0.29 / 27 ' nrs='0.29 / 27 ' sa=0 sb=0 sd=0 mult=1 m=1
.ends


* expanding   symbol:  Gm_C_LPF.sym # of pins=9
** sym_path: xschem/Gm_C_LPF.sym
** sch_path: xschem/Gm_C_LPF.sch
.subckt Gm_C_LPF Vdd Vss Vg+ Vg- IoutA IoutB V+ V- Ibias
*.ipin V-
*.ipin V+
*.ipin Vdd
*.ipin Vss
*.ipin Ibias
*.ipin Vg-
*.ipin Vg+
*.iopin IoutA
*.iopin IoutB
XM1 net2 Ibias Vdd Vdd sky130_fd_pr__pfet_g5v0d10v5 L=3 W=31 nf=8 ad='int((8 + 1)/2) * 31 / 8 * 0.29'
+ as='int((8 + 2)/2) * 31 / 8 * 0.29' pd='2*int((8 + 1)/2) * (31 / 8 + 0.29)' ps='2*int((8 + 2)/2) * (31 / 8 + 0.29)'
+ nrd='0.29 / 31 ' nrs='0.29 / 31 ' sa=0 sb=0 sd=0 mult=1 m=1
XM2 net3 V- net2 Vdd sky130_fd_pr__pfet_g5v0d10v5 L=3 W=40 nf=4 ad='int((4 + 1)/2) * 40 / 4 * 0.29' as='int((4 + 2)/2) * 40 / 4 * 0.29'
+ pd='2*int((4 + 1)/2) * (40 / 4 + 0.29)' ps='2*int((4 + 2)/2) * (40 / 4 + 0.29)' nrd='0.29 / 40 ' nrs='0.29 / 40 '
+ sa=0 sb=0 sd=0 mult=4 m=4
XM3 net4 V+ net1 Vdd sky130_fd_pr__pfet_g5v0d10v5 L=3 W=40 nf=4 ad='int((4 + 1)/2) * 40 / 4 * 0.29' as='int((4 + 2)/2) * 40 / 4 * 0.29'
+ pd='2*int((4 + 1)/2) * (40 / 4 + 0.29)' ps='2*int((4 + 2)/2) * (40 / 4 + 0.29)' nrd='0.29 / 40 ' nrs='0.29 / 40 '
+ sa=0 sb=0 sd=0 mult=4 m=4
XM4 net6 net3 Vss Vss sky130_fd_pr__nfet_g5v0d10v5 L=6 W=1 nf=1 ad='int((1 + 1)/2) * 1 / 1 * 0.29' as='int((1 + 2)/2) * 1 / 1 * 0.29'
+ pd='2*int((1 + 1)/2) * (1 / 1 + 0.29)' ps='2*int((1 + 2)/2) * (1 / 1 + 0.29)' nrd='0.29 / 1 ' nrs='0.29 / 1 '
+ sa=0 sb=0 sd=0 mult=4 m=4
XM5 net7 net4 Vss Vss sky130_fd_pr__nfet_g5v0d10v5 L=6 W=1 nf=1 ad='int((1 + 1)/2) * 1 / 1 * 0.29' as='int((1 + 2)/2) * 1 / 1 * 0.29'
+ pd='2*int((1 + 1)/2) * (1 / 1 + 0.29)' ps='2*int((1 + 2)/2) * (1 / 1 + 0.29)' nrd='0.29 / 1 ' nrs='0.29 / 1 '
+ sa=0 sb=0 sd=0 mult=4 m=4
XM6 net9 net3 Vss Vss sky130_fd_pr__nfet_g5v0d10v5 L=6 W=1 nf=1 ad='int((1 + 1)/2) * 1 / 1 * 0.29' as='int((1 + 2)/2) * 1 / 1 * 0.29'
+ pd='2*int((1 + 1)/2) * (1 / 1 + 0.29)' ps='2*int((1 + 2)/2) * (1 / 1 + 0.29)' nrd='0.29 / 1 ' nrs='0.29 / 1 '
+ sa=0 sb=0 sd=0 mult=4 m=4
XM7 net10 net4 Vss Vss sky130_fd_pr__nfet_g5v0d10v5 L=6 W=1 nf=1 ad='int((1 + 1)/2) * 1 / 1 * 0.29' as='int((1 + 2)/2) * 1 / 1 * 0.29'
+ pd='2*int((1 + 1)/2) * (1 / 1 + 0.29)' ps='2*int((1 + 2)/2) * (1 / 1 + 0.29)' nrd='0.29 / 1 ' nrs='0.29 / 1 '
+ sa=0 sb=0 sd=0 mult=4 m=4
XM8 net5 net5 Vdd Vdd sky130_fd_pr__pfet_g5v0d10v5 L=3 W=40 nf=4 ad='int((4 + 1)/2) * 40 / 4 * 0.29'
+ as='int((4 + 2)/2) * 40 / 4 * 0.29' pd='2*int((4 + 1)/2) * (40 / 4 + 0.29)' ps='2*int((4 + 2)/2) * (40 / 4 + 0.29)'
+ nrd='0.29 / 40 ' nrs='0.29 / 40 ' sa=0 sb=0 sd=0 mult=4 m=4
XM9 IoutA net5 Vdd Vdd sky130_fd_pr__pfet_g5v0d10v5 L=3 W=40 nf=4 ad='int((4 + 1)/2) * 40 / 4 * 0.29'
+ as='int((4 + 2)/2) * 40 / 4 * 0.29' pd='2*int((4 + 1)/2) * (40 / 4 + 0.29)' ps='2*int((4 + 2)/2) * (40 / 4 + 0.29)'
+ nrd='0.29 / 40 ' nrs='0.29 / 40 ' sa=0 sb=0 sd=0 mult=4 m=4
XM10 net1 Ibias Vdd Vdd sky130_fd_pr__pfet_g5v0d10v5 L=3 W=31 nf=8 ad='int((8 + 1)/2) * 31 / 8 * 0.29'
+ as='int((8 + 2)/2) * 31 / 8 * 0.29' pd='2*int((8 + 1)/2) * (31 / 8 + 0.29)' ps='2*int((8 + 2)/2) * (31 / 8 + 0.29)'
+ nrd='0.29 / 31 ' nrs='0.29 / 31 ' sa=0 sb=0 sd=0 mult=1 m=1
XM11 net3 Vg+ net6 Vss sky130_fd_pr__nfet_g5v0d10v5 L=6 W=1 nf=1 ad='int((1 + 1)/2) * 1 / 1 * 0.29' as='int((1 + 2)/2) * 1 / 1 * 0.29'
+ pd='2*int((1 + 1)/2) * (1 / 1 + 0.29)' ps='2*int((1 + 2)/2) * (1 / 1 + 0.29)' nrd='0.29 / 1 ' nrs='0.29 / 1 '
+ sa=0 sb=0 sd=0 mult=2 m=2
XM12 net3 Vg- net6 Vss sky130_fd_pr__nfet_g5v0d10v5 L=6 W=1 nf=1 ad='int((1 + 1)/2) * 1 / 1 * 0.29' as='int((1 + 2)/2) * 1 / 1 * 0.29'
+ pd='2*int((1 + 1)/2) * (1 / 1 + 0.29)' ps='2*int((1 + 2)/2) * (1 / 1 + 0.29)' nrd='0.29 / 1 ' nrs='0.29 / 1 '
+ sa=0 sb=0 sd=0 mult=2 m=2
XM13 net4 Vg- net7 Vss sky130_fd_pr__nfet_g5v0d10v5 L=6 W=1 nf=1 ad='int((1 + 1)/2) * 1 / 1 * 0.29' as='int((1 + 2)/2) * 1 / 1 * 0.29'
+ pd='2*int((1 + 1)/2) * (1 / 1 + 0.29)' ps='2*int((1 + 2)/2) * (1 / 1 + 0.29)' nrd='0.29 / 1 ' nrs='0.29 / 1 '
+ sa=0 sb=0 sd=0 mult=2 m=2
XM14 net4 Vg+ net7 Vss sky130_fd_pr__nfet_g5v0d10v5 L=6 W=1 nf=1 ad='int((1 + 1)/2) * 1 / 1 * 0.29' as='int((1 + 2)/2) * 1 / 1 * 0.29'
+ pd='2*int((1 + 1)/2) * (1 / 1 + 0.29)' ps='2*int((1 + 2)/2) * (1 / 1 + 0.29)' nrd='0.29 / 1 ' nrs='0.29 / 1 '
+ sa=0 sb=0 sd=0 mult=2 m=2
XM16 net8 net8 Vdd Vdd sky130_fd_pr__pfet_g5v0d10v5 L=3 W=40 nf=4 ad='int((4 + 1)/2) * 40 / 4 * 0.29'
+ as='int((4 + 2)/2) * 40 / 4 * 0.29' pd='2*int((4 + 1)/2) * (40 / 4 + 0.29)' ps='2*int((4 + 2)/2) * (40 / 4 + 0.29)'
+ nrd='0.29 / 40 ' nrs='0.29 / 40 ' sa=0 sb=0 sd=0 mult=4 m=4
XM17 IoutB net8 Vdd Vdd sky130_fd_pr__pfet_g5v0d10v5 L=3 W=40 nf=4 ad='int((4 + 1)/2) * 40 / 4 * 0.29'
+ as='int((4 + 2)/2) * 40 / 4 * 0.29' pd='2*int((4 + 1)/2) * (40 / 4 + 0.29)' ps='2*int((4 + 2)/2) * (40 / 4 + 0.29)'
+ nrd='0.29 / 40 ' nrs='0.29 / 40 ' sa=0 sb=0 sd=0 mult=4 m=4
XM15 net8 Vg- net9 Vss sky130_fd_pr__nfet_g5v0d10v5 L=6 W=1 nf=1 ad='int((1 + 1)/2) * 1 / 1 * 0.29' as='int((1 + 2)/2) * 1 / 1 * 0.29'
+ pd='2*int((1 + 1)/2) * (1 / 1 + 0.29)' ps='2*int((1 + 2)/2) * (1 / 1 + 0.29)' nrd='0.29 / 1 ' nrs='0.29 / 1 '
+ sa=0 sb=0 sd=0 mult=2 m=2
XM18 net5 Vg+ net9 Vss sky130_fd_pr__nfet_g5v0d10v5 L=6 W=1 nf=1 ad='int((1 + 1)/2) * 1 / 1 * 0.29' as='int((1 + 2)/2) * 1 / 1 * 0.29'
+ pd='2*int((1 + 1)/2) * (1 / 1 + 0.29)' ps='2*int((1 + 2)/2) * (1 / 1 + 0.29)' nrd='0.29 / 1 ' nrs='0.29 / 1 '
+ sa=0 sb=0 sd=0 mult=2 m=2
XM19 IoutA Vg+ net10 Vss sky130_fd_pr__nfet_g5v0d10v5 L=6 W=1 nf=1 ad='int((1 + 1)/2) * 1 / 1 * 0.29'
+ as='int((1 + 2)/2) * 1 / 1 * 0.29' pd='2*int((1 + 1)/2) * (1 / 1 + 0.29)' ps='2*int((1 + 2)/2) * (1 / 1 + 0.29)'
+ nrd='0.29 / 1 ' nrs='0.29 / 1 ' sa=0 sb=0 sd=0 mult=2 m=2
XM20 IoutB Vg- net10 Vss sky130_fd_pr__nfet_g5v0d10v5 L=6 W=1 nf=1 ad='int((1 + 1)/2) * 1 / 1 * 0.29'
+ as='int((1 + 2)/2) * 1 / 1 * 0.29' pd='2*int((1 + 1)/2) * (1 / 1 + 0.29)' ps='2*int((1 + 2)/2) * (1 / 1 + 0.29)'
+ nrd='0.29 / 1 ' nrs='0.29 / 1 ' sa=0 sb=0 sd=0 mult=2 m=2
XM21 net1 V- net2 Vdd sky130_fd_pr__pfet_g5v0d10v5 L=3 W=24 nf=4 ad='int((4 + 1)/2) * 24 / 4 * 0.29'
+ as='int((4 + 2)/2) * 24 / 4 * 0.29' pd='2*int((4 + 1)/2) * (24 / 4 + 0.29)' ps='2*int((4 + 2)/2) * (24 / 4 + 0.29)'
+ nrd='0.29 / 24 ' nrs='0.29 / 24 ' sa=0 sb=0 sd=0 mult=1 m=1
XM22 net2 V+ net1 Vdd sky130_fd_pr__pfet_g5v0d10v5 L=3 W=24 nf=4 ad='int((4 + 1)/2) * 24 / 4 * 0.29'
+ as='int((4 + 2)/2) * 24 / 4 * 0.29' pd='2*int((4 + 1)/2) * (24 / 4 + 0.29)' ps='2*int((4 + 2)/2) * (24 / 4 + 0.29)'
+ nrd='0.29 / 24 ' nrs='0.29 / 24 ' sa=0 sb=0 sd=0 mult=1 m=1
.ends


* expanding   symbol:  NAND_GATE.sym # of pins=5
** sym_path: xschem/NAND_GATE.sym
** sch_path: xschem/NAND_GATE.sch
.subckt NAND_GATE Vdd A B Vout Vss
*.ipin Vdd
*.ipin Vss
*.ipin A
*.ipin B
*.opin Vout
XM3 Vout A net1 Vss sky130_fd_pr__nfet_g5v0d10v5 L=0.5 W=1 nf=1 ad='int((1 + 1)/2) * 1 / 1 * 0.29' as='int((1 + 2)/2) * 1 / 1 * 0.29'
+ pd='2*int((1 + 1)/2) * (1 / 1 + 0.29)' ps='2*int((1 + 2)/2) * (1 / 1 + 0.29)' nrd='0.29 / 1 ' nrs='0.29 / 1 '
+ sa=0 sb=0 sd=0 mult=1 m=1
XM4 Vout A Vdd Vdd sky130_fd_pr__pfet_g5v0d10v5 L=0.5 W=3 nf=1 ad='int((1 + 1)/2) * 3 / 1 * 0.29' as='int((1 + 2)/2) * 3 / 1 * 0.29'
+ pd='2*int((1 + 1)/2) * (3 / 1 + 0.29)' ps='2*int((1 + 2)/2) * (3 / 1 + 0.29)' nrd='0.29 / 3 ' nrs='0.29 / 3 '
+ sa=0 sb=0 sd=0 mult=1 m=1
XM5 Vout B Vdd Vdd sky130_fd_pr__pfet_g5v0d10v5 L=0.5 W=3 nf=1 ad='int((1 + 1)/2) * 3 / 1 * 0.29' as='int((1 + 2)/2) * 3 / 1 * 0.29'
+ pd='2*int((1 + 1)/2) * (3 / 1 + 0.29)' ps='2*int((1 + 2)/2) * (3 / 1 + 0.29)' nrd='0.29 / 3 ' nrs='0.29 / 3 '
+ sa=0 sb=0 sd=0 mult=1 m=1
XM1 net1 B Vss Vss sky130_fd_pr__nfet_g5v0d10v5 L=0.5 W=1 nf=1 ad='int((1 + 1)/2) * 1 / 1 * 0.29' as='int((1 + 2)/2) * 1 / 1 * 0.29'
+ pd='2*int((1 + 1)/2) * (1 / 1 + 0.29)' ps='2*int((1 + 2)/2) * (1 / 1 + 0.29)' nrd='0.29 / 1 ' nrs='0.29 / 1 '
+ sa=0 sb=0 sd=0 mult=1 m=1
.ends

.GLOBAL GND
.end
